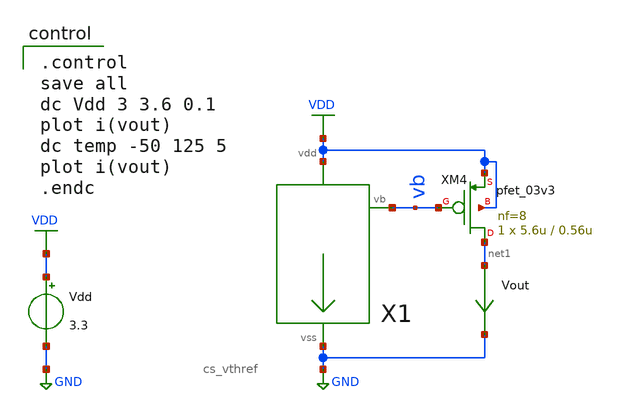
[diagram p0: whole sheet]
** sch_path: BGR/xschem/tbdc_cs_vthref.sch
**.subckt tbdc_cs_vthref
Vdd VDD GND 3.3
X1 GND VDD vb cs_vthref
XM4 net1 vb VDD VDD pfet_03v3 L=0.56u W=5.6u nf=8 ad='int((nf+1)/2) * W/nf * 0.18u' as='int((nf+2)/2) * W/nf * 0.18u'
+ pd='2*int((nf+1)/2) * (W/nf + 0.18u)' ps='2*int((nf+2)/2) * (W/nf + 0.18u)' nrd='0.18u / W' nrs='0.18u / W'
+ sa=0 sb=0 sd=0 m=1
Vout net1 GND 0
.save i(vout)
**** begin user architecture code

.include $::180MCU_MODELS/design.ngspice
.lib $::180MCU_MODELS/sm141064.ngspice typical
.lib $::180MCU_MODELS/sm141064.ngspice res_typical
.lib $::180MCU_MODELS/sm141064.ngspice moscap_typical
.lib $::180MCU_MODELS/sm141064.ngspice bjt_typical
* .lib $::180MCU_MODELS/sm141064.ngspice res_statistical


.control
save all
dc Vdd 3 3.6 0.1
plot i(vout)
dc temp -50 125 5
plot i(vout)
.endc

**** end user architecture code
**.ends
.GLOBAL GND
.GLOBAL VDD
.end
